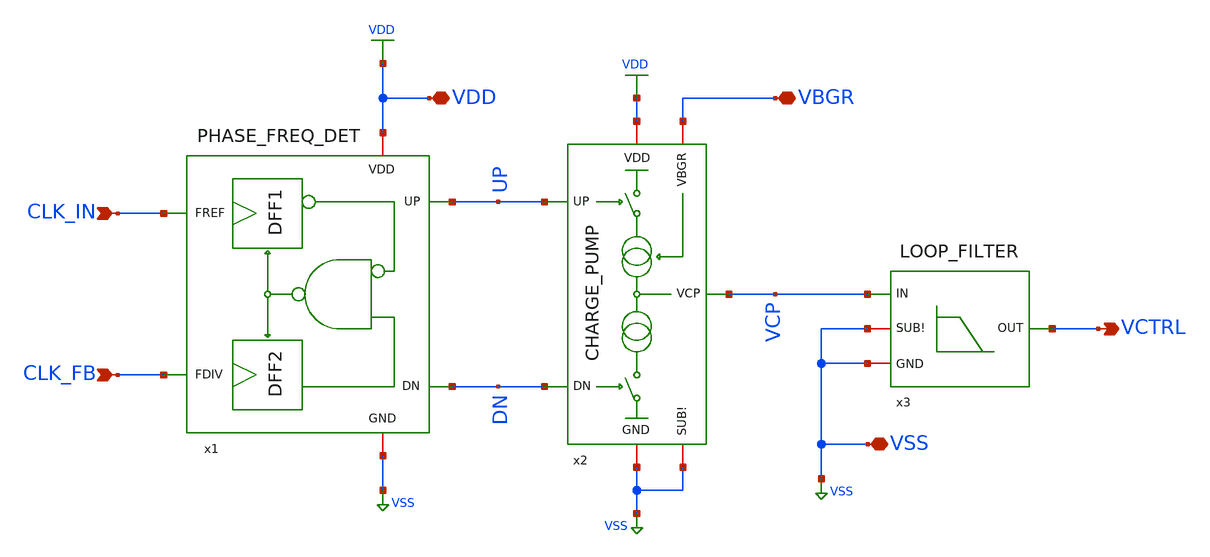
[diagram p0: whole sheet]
** sch_path: xschem/PFD_CP_LF.sch
**.subckt PFD_CP_LF CLK_IN VCTRL VDD VSS CLK_FB VBGR
*.ipin CLK_IN
*.opin VCTRL
*.iopin VDD
*.iopin VSS
*.ipin CLK_FB
*.iopin VBGR
x1 CLK_IN UP VDD VSS CLK_FB DN PHASE_FREQ_DET
x2 UP VDD VCP VBGR VSS DN VSS CHARGE_PUMP
x3 VCTRL VCP VSS VSS LOOP_FILTER
**.ends
.GLOBAL VSS
.GLOBAL VDD
.end
